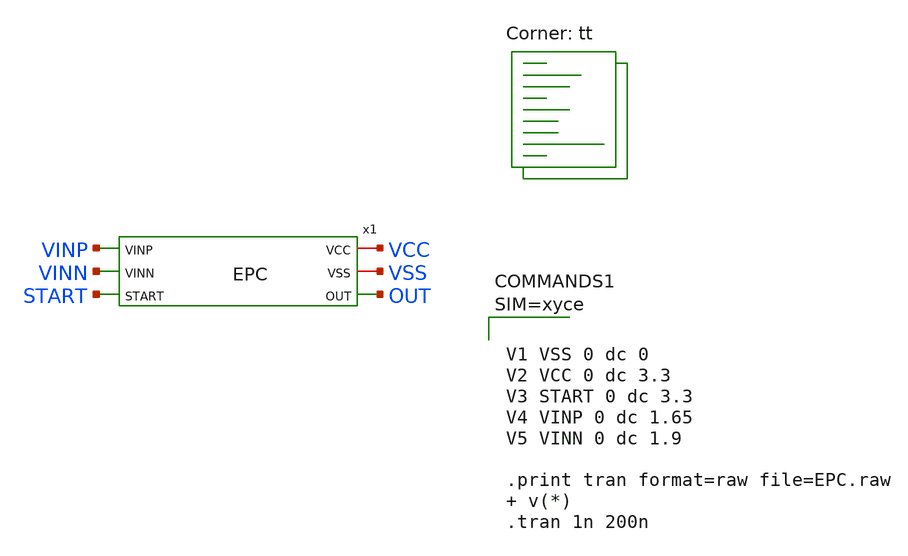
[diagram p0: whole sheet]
** sch_path: Comparator/schematic/Edge_pursuit_comparator/EPC_testbench.sch
**.subckt EPC_testbench
x1 VCC VSS VINP VINN START OUT EPC
**** begin user architecture code
.lib $::SKYWATER_MODELS/sky130.lib.spice tt



**** end user architecture code
**.ends

* expanding   symbol:  /foss/designs/Comparator/schematic/Edge_pursuit_comparator/EPC.sym # of
*+ pins=6
** sym_path: Comparator/schematic/Edge_pursuit_comparator/EPC.sym
** sch_path: Comparator/schematic/Edge_pursuit_comparator/EPC.sch
.subckt EPC VCC VSS VINP VINN START OUT
*.iopin VCC
*.opin OUT
*.ipin VINN
*.iopin VSS
*.ipin VINP
*.ipin START
x1 VCC VSS net8 VINP VINP net1 delay_cell
x2 VCC VSS net1 VINN VINN net2 delay_cell
x3 VCC VSS net2 VINP VINP net3 delay_cell
x4 VCC VSS net3 VINN VINN OUT delay_cell
x5 VCC VSS net4 VINP VINP net9 delay_cell
x6 VCC VSS net5 VINN VINN net4 delay_cell
x7 VCC VSS net6 VINP VINP net5 delay_cell
x8 VCC VSS net7 VINN VINN net6 delay_cell
x9 VCC VSS OUT START net7 nand
x10 VCC VSS START net9 net8 nand
.ends


* expanding   symbol:  /foss/designs/Comparator/schematic/Edge_pursuit_comparator/delay_cell.sym #
*+ of pins=6
** sym_path: Comparator/schematic/Edge_pursuit_comparator/delay_cell.sym
** sch_path: Comparator/schematic/Edge_pursuit_comparator/delay_cell.sch
.subckt delay_cell VCC VSS IN VINP VINN OUT
*.iopin VCC
*.opin OUT
*.ipin VINP
*.ipin VINN
*.iopin VSS
*.ipin IN
XM1 OUT IN net1 VCC sky130_fd_pr__pfet_g5v0d10v5 L=0.5 W=1 nf=1 ad='int((nf+1)/2) * W/nf * 0.29' as='int((nf+2)/2) * W/nf * 0.29'
+ pd='2*int((nf+1)/2) * (W/nf + 0.29)' ps='2*int((nf+2)/2) * (W/nf + 0.29)' nrd='0.29 / W' nrs='0.29 / W'
+ sa=0 sb=0 sd=0 mult=1 m=1
XM2 OUT IN net2 VSS sky130_fd_pr__nfet_g5v0d10v5 L=0.5 W=1 nf=1 ad='int((nf+1)/2) * W/nf * 0.29' as='int((nf+2)/2) * W/nf * 0.29'
+ pd='2*int((nf+1)/2) * (W/nf + 0.29)' ps='2*int((nf+2)/2) * (W/nf + 0.29)' nrd='0.29 / W' nrs='0.29 / W'
+ sa=0 sb=0 sd=0 mult=1 m=1
XM3 net2 VINN VSS VSS sky130_fd_pr__nfet_g5v0d10v5 L=0.5 W=1 nf=1 ad='int((nf+1)/2) * W/nf * 0.29' as='int((nf+2)/2) * W/nf * 0.29'
+ pd='2*int((nf+1)/2) * (W/nf + 0.29)' ps='2*int((nf+2)/2) * (W/nf + 0.29)' nrd='0.29 / W' nrs='0.29 / W'
+ sa=0 sb=0 sd=0 mult=1 m=1
XM4 net1 VINP VCC VCC sky130_fd_pr__pfet_g5v0d10v5 L=0.5 W=1 nf=1 ad='int((nf+1)/2) * W/nf * 0.29' as='int((nf+2)/2) * W/nf * 0.29'
+ pd='2*int((nf+1)/2) * (W/nf + 0.29)' ps='2*int((nf+2)/2) * (W/nf + 0.29)' nrd='0.29 / W' nrs='0.29 / W'
+ sa=0 sb=0 sd=0 mult=1 m=1
.ends


* expanding   symbol:  /foss/designs/Comparator/schematic/Edge_pursuit_comparator/nand.sym # of
*+ pins=5
** sym_path: Comparator/schematic/Edge_pursuit_comparator/nand.sym
** sch_path: Comparator/schematic/Edge_pursuit_comparator/nand.sch
.subckt nand VCC VSS A B OUT
*.iopin VCC
*.opin OUT
*.ipin B
*.iopin VSS
*.ipin A
XM1 OUT B VCC VCC sky130_fd_pr__pfet_g5v0d10v5 L=0.5 W=1 nf=1 ad='int((nf+1)/2) * W/nf * 0.29' as='int((nf+2)/2) * W/nf * 0.29'
+ pd='2*int((nf+1)/2) * (W/nf + 0.29)' ps='2*int((nf+2)/2) * (W/nf + 0.29)' nrd='0.29 / W' nrs='0.29 / W'
+ sa=0 sb=0 sd=0 mult=1 m=1
XM2 OUT A net1 VSS sky130_fd_pr__nfet_g5v0d10v5 L=0.5 W=1 nf=1 ad='int((nf+1)/2) * W/nf * 0.29' as='int((nf+2)/2) * W/nf * 0.29'
+ pd='2*int((nf+1)/2) * (W/nf + 0.29)' ps='2*int((nf+2)/2) * (W/nf + 0.29)' nrd='0.29 / W' nrs='0.29 / W'
+ sa=0 sb=0 sd=0 mult=1 m=1
XM3 net1 B VSS VSS sky130_fd_pr__nfet_g5v0d10v5 L=0.5 W=1 nf=1 ad='int((nf+1)/2) * W/nf * 0.29' as='int((nf+2)/2) * W/nf * 0.29'
+ pd='2*int((nf+1)/2) * (W/nf + 0.29)' ps='2*int((nf+2)/2) * (W/nf + 0.29)' nrd='0.29 / W' nrs='0.29 / W'
+ sa=0 sb=0 sd=0 mult=1 m=1
XM4 OUT A VCC VCC sky130_fd_pr__pfet_g5v0d10v5 L=0.5 W=1 nf=1 ad='int((nf+1)/2) * W/nf * 0.29' as='int((nf+2)/2) * W/nf * 0.29'
+ pd='2*int((nf+1)/2) * (W/nf + 0.29)' ps='2*int((nf+2)/2) * (W/nf + 0.29)' nrd='0.29 / W' nrs='0.29 / W'
+ sa=0 sb=0 sd=0 mult=1 m=1
.ends

.end
